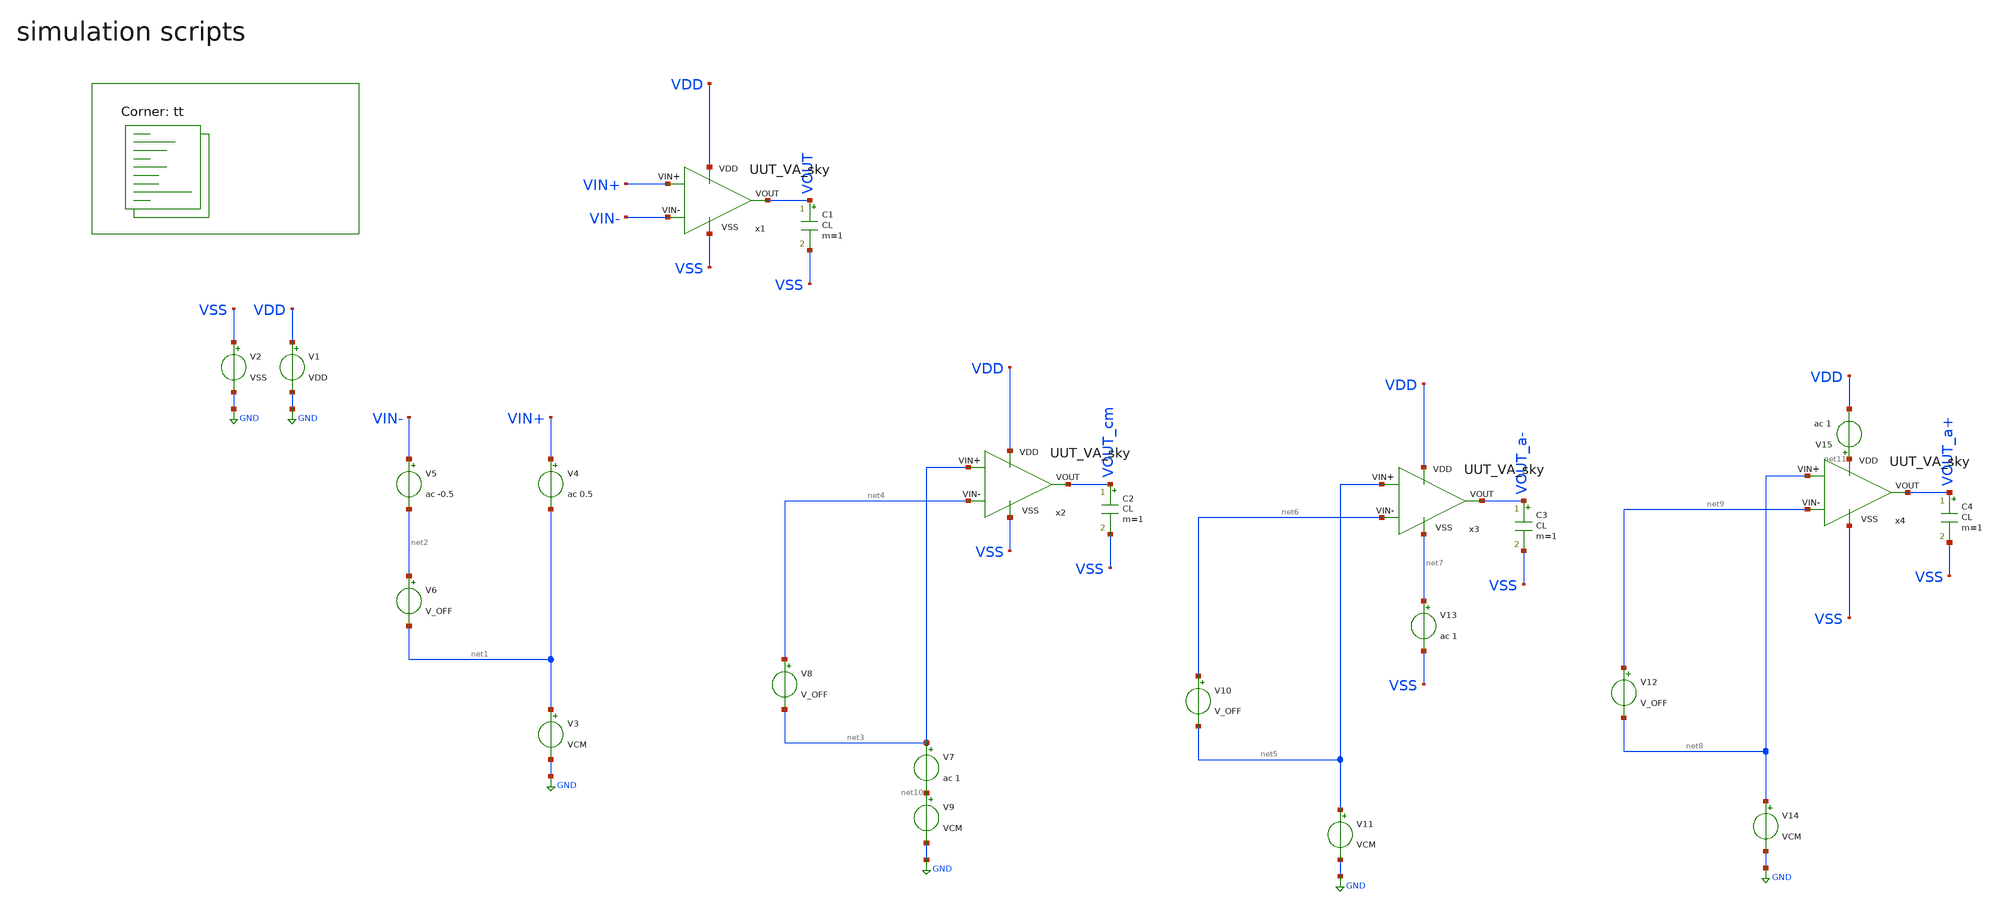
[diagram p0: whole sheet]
** sch_path: Learning/single_ended_amplifiers/Design_and_Analysis_of_Two-Stage_CMOS_Operational_Amplifier_for_Fluorescence_Signal_Processing_sky130_5V/amplifier_design/OTA_AC_TB.sch
**.subckt OTA_AC_TB
V1 VDD GND VDD
V2 VSS GND VSS
V4 VIN+ net1 ac 0.5
V6 net2 net1 V_OFF
V3 net1 GND VCM
V5 VIN- net2 ac -0.5
C1 VOUT VSS CL m=1
C2 VOUT_cm VSS CL m=1
V8 net4 net3 V_OFF
V9 net10 GND VCM
V7 net3 net10 ac 1
C3 VOUT_a- VSS CL m=1
V10 net6 net5 V_OFF
V11 net5 GND VCM
V13 net7 VSS ac 1
C4 VOUT_a+ VSS CL m=1
V12 net9 net8 V_OFF
V14 net8 GND VCM
V15 net11 VDD ac 1
x1 VDD VSS VIN- VIN+ VOUT UUT_VA_sky
x2 VDD VSS net4 net3 VOUT_cm UUT_VA_sky
x3 VDD net7 net6 net5 VOUT_a- UUT_VA_sky
x4 net11 VSS net9 net8 VOUT_a+ UUT_VA_sky
**** begin user architecture code
.lib $::SKYWATER_MODELS/sky130.lib.spice tt

.Temp 27
.param VDD = 1.8
.param VSS = 0
.param VCM={(VDD-VSS)/2}
.param VCM_NEG={-VCM}
.param V_OFF = 2.01u
.param CL = 3p

.control
save all

ac dec 100 1 10G
setseed 10
wrdata VIN_sweep_AC.csv db(v(VOUT)) phase(VOUT) db(v(VOUT_cm)) db(v(VOUT_a-)) db(v(VOUT_a+))
plot db(v(VOUT)) phase(VOUT)
plot db(v(VOUT_cm))
plot db(v(VOUT_a-))
plot db(v(VOUT_a+))

.endc

**** end user architecture code
**.ends

* expanding   symbol:  Sky130A/UUT_sky/UUT_VA_sky.sym # of pins=5
** sym_path: my_ip/LIB/Sky130A/UUT_sky/UUT_VA_sky.sym
** sch_path: my_ip/LIB/Sky130A/UUT_sky/UUT_VA_sky.sch
.subckt UUT_VA_sky VDD VSS VIN- VIN+ VOUT
*.iopin VDD
*.iopin VSS
*.iopin VIN-
*.iopin VIN+
*.iopin VOUT
x1 VDD VSS VIN+ VIN- VOUT amplifier
.ends


* expanding   symbol:
*+  Sky130A/Learning/Design_of_Two-Stage_CMOS_Operational_Amplifier_for_Fluorescence_Signal_Processing_5V/amplifier.sym # of pins=5
** sym_path: my_ip/LIB/Sky130A/Learning/Design_of_Two-Stage_CMOS_Operational_Amplifier_for_Fluorescence_Signal_Processing_5V/amplifier.sym
** sch_path: my_ip/LIB/Sky130A/Learning/Design_of_Two-Stage_CMOS_Operational_Amplifier_for_Fluorescence_Signal_Processing_5V/amplifier.sch
.subckt amplifier VDD VSS Vin+ Vin- VOUT
*.iopin VDD
*.iopin VSS
*.iopin Vin+
*.iopin Vin-
*.iopin VOUT
XR2 VSS net2 VSS sky130_fd_pr__res_high_po_0p35 L=20.4 mult=1 m=1
XM7 net1 net1 VSS VSS sky130_fd_pr__nfet_g5v0d10v5 L=3.2 W='1 * 2 ' nf=2 ad='int((nf+1)/2) * W / nf * 0.29'
+ as='int((nf+2)/2) * W / nf * 0.29' pd='2*int((nf+1)/2) * (W / nf + 0.29)' ps='2*int((nf+2)/2) * (W / nf + 0.29)'
+ nrd='0.29 / W ' nrs='0.29 / W ' sa=0 sb=0 sd=0 mult=2 m=2
XM8 net3 net1 net2 VSS sky130_fd_pr__nfet_g5v0d10v5 L=3.2 W='1 * 8 ' nf=8 ad='int((nf+1)/2) * W / nf * 0.29'
+ as='int((nf+2)/2) * W / nf * 0.29' pd='2*int((nf+1)/2) * (W / nf + 0.29)' ps='2*int((nf+2)/2) * (W / nf + 0.29)'
+ nrd='0.29 / W ' nrs='0.29 / W ' sa=0 sb=0 sd=0 mult=2 m=2
XM9 VB1 VB2 net3 VSS sky130_fd_pr__nfet_g5v0d10v5 L=2 W='1 * 2 ' nf=2 ad='int((nf+1)/2) * W / nf * 0.29'
+ as='int((nf+2)/2) * W / nf * 0.29' pd='2*int((nf+1)/2) * (W / nf + 0.29)' ps='2*int((nf+2)/2) * (W / nf + 0.29)'
+ nrd='0.29 / W ' nrs='0.29 / W ' sa=0 sb=0 sd=0 mult=2 m=2
XM10 VB2 VB2 net1 VSS sky130_fd_pr__nfet_g5v0d10v5 L=2 W='1 * 2 ' nf=2 ad='int((nf+1)/2) * W / nf * 0.29'
+ as='int((nf+2)/2) * W / nf * 0.29' pd='2*int((nf+1)/2) * (W / nf + 0.29)' ps='2*int((nf+2)/2) * (W / nf + 0.29)'
+ nrd='0.29 / W ' nrs='0.29 / W ' sa=0 sb=0 sd=0 mult=2 m=2
XM2 net6 Vin- net4 net4 sky130_fd_pr__pfet_g5v0d10v5 L=1 W='4.5 * 2 ' nf=2 ad='int((2 + 1)/2) * 4.5 * 0.29'
+ as='int((2 + 2)/2) * 4.5 * 0.29' pd='2*int((2 + 1)/2) * (4.5 + 0.29)' ps='2*int((2 + 2)/2) * (4.5 + 0.29)'
+ nrd='0.29 / 4.5 / 2 ' nrs='0.29 / 4.5 / 2 ' sa=0 sb=0 sd=0 mult=4 m=4
XM3 net5 Vin+ net4 net4 sky130_fd_pr__pfet_g5v0d10v5 L=1 W='4.5 * 2 ' nf=2 ad='int((2 + 1)/2) * 4.5 * 0.29'
+ as='int((2 + 2)/2) * 4.5 * 0.29' pd='2*int((2 + 1)/2) * (4.5 + 0.29)' ps='2*int((2 + 2)/2) * (4.5 + 0.29)'
+ nrd='0.29 / 4.5 / 2 ' nrs='0.29 / 4.5 / 2 ' sa=0 sb=0 sd=0 mult=4 m=4
XM4 net5 net6 VSS VSS sky130_fd_pr__nfet_g5v0d10v5 L=2 W='1.5 * 2 ' nf=2 ad='int((nf+1)/2) * W / nf * 0.29'
+ as='int((nf+2)/2) * W / nf * 0.29' pd='2*int((nf+1)/2) * (W / nf + 0.29)' ps='2*int((nf+2)/2) * (W / nf + 0.29)'
+ nrd='0.29 / W ' nrs='0.29 / W ' sa=0 sb=0 sd=0 mult=2 m=2
XM11 net6 net6 VSS VSS sky130_fd_pr__nfet_g5v0d10v5 L=2 W='1.5 * 2 ' nf=2 ad='int((nf+1)/2) * W / nf * 0.29'
+ as='int((nf+2)/2) * W / nf * 0.29' pd='2*int((nf+1)/2) * (W / nf + 0.29)' ps='2*int((nf+2)/2) * (W / nf + 0.29)'
+ nrd='0.29 / W ' nrs='0.29 / W ' sa=0 sb=0 sd=0 mult=2 m=2
XM13 VOUT net5 VSS VSS sky130_fd_pr__nfet_g5v0d10v5 L=1 W='4 * 2 ' nf=2 ad='int((nf+1)/2) * W / nf * 0.29'
+ as='int((nf+2)/2) * W / nf * 0.29' pd='2*int((nf+1)/2) * (W / nf + 0.29)' ps='2*int((nf+2)/2) * (W / nf + 0.29)'
+ nrd='0.29 / W ' nrs='0.29 / W ' sa=0 sb=0 sd=0 mult=2 m=2
XM14 net7 VB2 net5 VSS sky130_fd_pr__nfet_g5v0d10v5 L=2 W='1.4 * 1 ' nf=1 ad='int((nf+1)/2) * W / nf * 0.29'
+ as='int((nf+2)/2) * W / nf * 0.29' pd='2*int((nf+1)/2) * (W / nf + 0.29)' ps='2*int((nf+2)/2) * (W / nf + 0.29)'
+ nrd='0.29 / W ' nrs='0.29 / W ' sa=0 sb=0 sd=0 mult=2 m=2
XC1 VOUT net7 sky130_fd_pr__cap_mim_m3_1 W=8 L=8 MF=4 m=4
XM1 VB2 VB1 VDD VDD sky130_fd_pr__pfet_g5v0d10v5 L=2.2 W='1 * 2 ' nf=2 ad='int((2 + 1)/2) * 1 * 0.29'
+ as='int((2 + 2)/2) * 1 * 0.29' pd='2*int((2 + 1)/2) * (1 + 0.29)' ps='2*int((2 + 2)/2) * (1 + 0.29)'
+ nrd='0.29 / 1 / 2 ' nrs='0.29 / 1 / 2 ' sa=0 sb=0 sd=0 mult=2 m=2
XM5 VB1 VB1 VDD VDD sky130_fd_pr__pfet_g5v0d10v5 L=2.2 W='1 * 2 ' nf=2 ad='int((2 + 1)/2) * 1 * 0.29'
+ as='int((2 + 2)/2) * 1 * 0.29' pd='2*int((2 + 1)/2) * (1 + 0.29)' ps='2*int((2 + 2)/2) * (1 + 0.29)'
+ nrd='0.29 / 1 / 2 ' nrs='0.29 / 1 / 2 ' sa=0 sb=0 sd=0 mult=2 m=2
XM6 net4 VB1 VDD VDD sky130_fd_pr__pfet_g5v0d10v5 L=2.2 W='1 * 2 ' nf=2 ad='int((2 + 1)/2) * 1 * 0.29'
+ as='int((2 + 2)/2) * 1 * 0.29' pd='2*int((2 + 1)/2) * (1 + 0.29)' ps='2*int((2 + 2)/2) * (1 + 0.29)'
+ nrd='0.29 / 1 / 2 ' nrs='0.29 / 1 / 2 ' sa=0 sb=0 sd=0 mult=8 m=8
XM12 VOUT VB1 VDD VDD sky130_fd_pr__pfet_g5v0d10v5 L=2.2 W='1 * 2 ' nf=2 ad='int((2 + 1)/2) * 1 * 0.29'
+ as='int((2 + 2)/2) * 1 * 0.29' pd='2*int((2 + 1)/2) * (1 + 0.29)' ps='2*int((2 + 2)/2) * (1 + 0.29)'
+ nrd='0.29 / 1 / 2 ' nrs='0.29 / 1 / 2 ' sa=0 sb=0 sd=0 mult=16 m=16
.ends

.GLOBAL GND
.end
